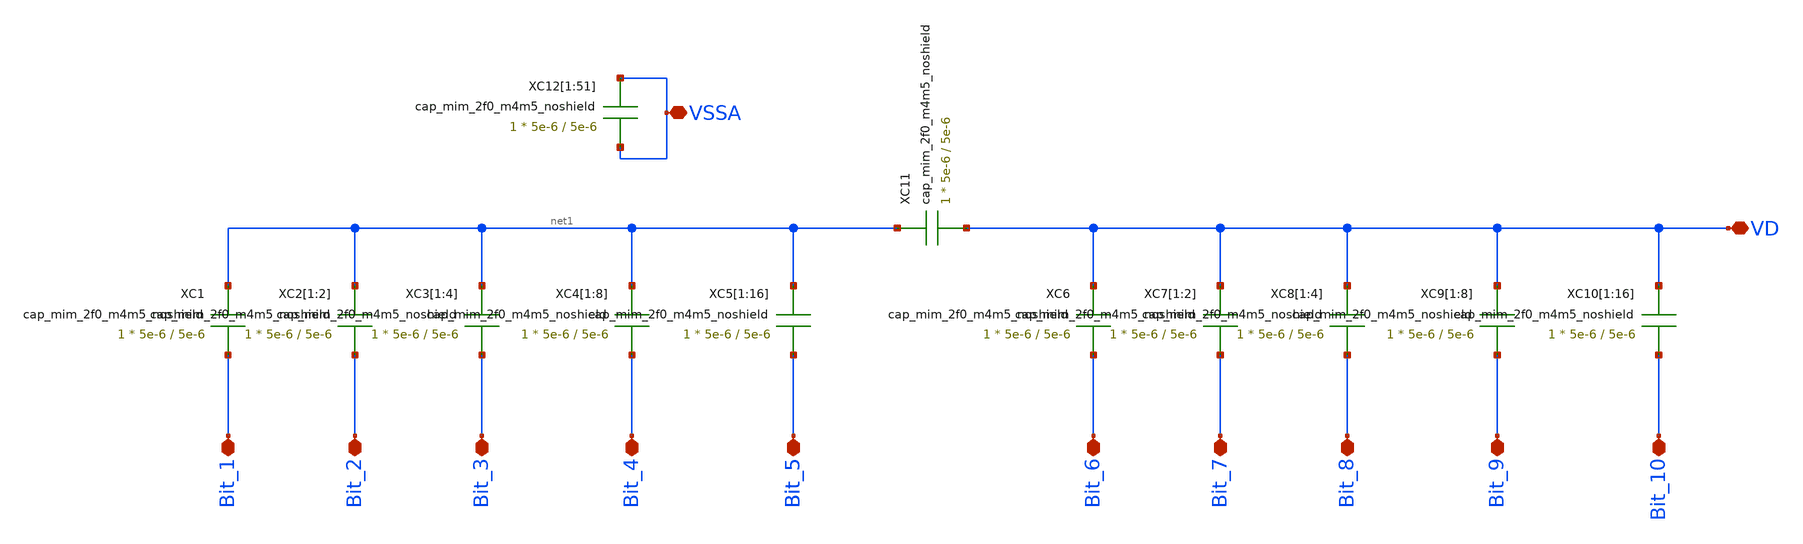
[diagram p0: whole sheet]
** sch_path: SAR_ADC/Differential_capacitive_DAC/xschem/Differential_capacitive_DAC_array.sch
**.subckt Differential_capacitive_DAC_array Bit_1 Bit_2 Bit_3 Bit_4 Bit_5 Bit_6 Bit_7 Bit_8 Bit_9
*+ Bit_10 VD Bit_5 VSSA
*.iopin Bit_1
*.iopin Bit_2
*.iopin Bit_3
*.iopin Bit_4
*.iopin Bit_5
*.iopin Bit_6
*.iopin Bit_7
*.iopin Bit_8
*.iopin Bit_9
*.iopin Bit_10
*.iopin VD
*.iopin Bit_5
*.iopin VSSA
XC1 net1 Bit_1 cap_mim_2f0_m4m5_noshield c_width=5e-6 c_length=5e-6 m=1
XC2[1] net1 Bit_2 cap_mim_2f0_m4m5_noshield c_width=5e-6 c_length=5e-6 m=1
XC2[2] net1 Bit_2 cap_mim_2f0_m4m5_noshield c_width=5e-6 c_length=5e-6 m=1
XC3[1] net1 Bit_3 cap_mim_2f0_m4m5_noshield c_width=5e-6 c_length=5e-6 m=1
XC3[2] net1 Bit_3 cap_mim_2f0_m4m5_noshield c_width=5e-6 c_length=5e-6 m=1
XC3[3] net1 Bit_3 cap_mim_2f0_m4m5_noshield c_width=5e-6 c_length=5e-6 m=1
XC3[4] net1 Bit_3 cap_mim_2f0_m4m5_noshield c_width=5e-6 c_length=5e-6 m=1
XC4[1] net1 Bit_4 cap_mim_2f0_m4m5_noshield c_width=5e-6 c_length=5e-6 m=1
XC4[2] net1 Bit_4 cap_mim_2f0_m4m5_noshield c_width=5e-6 c_length=5e-6 m=1
XC4[3] net1 Bit_4 cap_mim_2f0_m4m5_noshield c_width=5e-6 c_length=5e-6 m=1
XC4[4] net1 Bit_4 cap_mim_2f0_m4m5_noshield c_width=5e-6 c_length=5e-6 m=1
XC4[5] net1 Bit_4 cap_mim_2f0_m4m5_noshield c_width=5e-6 c_length=5e-6 m=1
XC4[6] net1 Bit_4 cap_mim_2f0_m4m5_noshield c_width=5e-6 c_length=5e-6 m=1
XC4[7] net1 Bit_4 cap_mim_2f0_m4m5_noshield c_width=5e-6 c_length=5e-6 m=1
XC4[8] net1 Bit_4 cap_mim_2f0_m4m5_noshield c_width=5e-6 c_length=5e-6 m=1
XC5[1] net1 Bit_5 cap_mim_2f0_m4m5_noshield c_width=5e-6 c_length=5e-6 m=1
XC5[2] net1 Bit_5 cap_mim_2f0_m4m5_noshield c_width=5e-6 c_length=5e-6 m=1
XC5[3] net1 Bit_5 cap_mim_2f0_m4m5_noshield c_width=5e-6 c_length=5e-6 m=1
XC5[4] net1 Bit_5 cap_mim_2f0_m4m5_noshield c_width=5e-6 c_length=5e-6 m=1
XC5[5] net1 Bit_5 cap_mim_2f0_m4m5_noshield c_width=5e-6 c_length=5e-6 m=1
XC5[6] net1 Bit_5 cap_mim_2f0_m4m5_noshield c_width=5e-6 c_length=5e-6 m=1
XC5[7] net1 Bit_5 cap_mim_2f0_m4m5_noshield c_width=5e-6 c_length=5e-6 m=1
XC5[8] net1 Bit_5 cap_mim_2f0_m4m5_noshield c_width=5e-6 c_length=5e-6 m=1
XC5[9] net1 Bit_5 cap_mim_2f0_m4m5_noshield c_width=5e-6 c_length=5e-6 m=1
XC5[10] net1 Bit_5 cap_mim_2f0_m4m5_noshield c_width=5e-6 c_length=5e-6 m=1
XC5[11] net1 Bit_5 cap_mim_2f0_m4m5_noshield c_width=5e-6 c_length=5e-6 m=1
XC5[12] net1 Bit_5 cap_mim_2f0_m4m5_noshield c_width=5e-6 c_length=5e-6 m=1
XC5[13] net1 Bit_5 cap_mim_2f0_m4m5_noshield c_width=5e-6 c_length=5e-6 m=1
XC5[14] net1 Bit_5 cap_mim_2f0_m4m5_noshield c_width=5e-6 c_length=5e-6 m=1
XC5[15] net1 Bit_5 cap_mim_2f0_m4m5_noshield c_width=5e-6 c_length=5e-6 m=1
XC5[16] net1 Bit_5 cap_mim_2f0_m4m5_noshield c_width=5e-6 c_length=5e-6 m=1
XC6 VD Bit_6 cap_mim_2f0_m4m5_noshield c_width=5e-6 c_length=5e-6 m=1
XC7[1] VD Bit_7 cap_mim_2f0_m4m5_noshield c_width=5e-6 c_length=5e-6 m=1
XC7[2] VD Bit_7 cap_mim_2f0_m4m5_noshield c_width=5e-6 c_length=5e-6 m=1
XC8[1] VD Bit_8 cap_mim_2f0_m4m5_noshield c_width=5e-6 c_length=5e-6 m=1
XC8[2] VD Bit_8 cap_mim_2f0_m4m5_noshield c_width=5e-6 c_length=5e-6 m=1
XC8[3] VD Bit_8 cap_mim_2f0_m4m5_noshield c_width=5e-6 c_length=5e-6 m=1
XC8[4] VD Bit_8 cap_mim_2f0_m4m5_noshield c_width=5e-6 c_length=5e-6 m=1
XC9[1] VD Bit_9 cap_mim_2f0_m4m5_noshield c_width=5e-6 c_length=5e-6 m=1
XC9[2] VD Bit_9 cap_mim_2f0_m4m5_noshield c_width=5e-6 c_length=5e-6 m=1
XC9[3] VD Bit_9 cap_mim_2f0_m4m5_noshield c_width=5e-6 c_length=5e-6 m=1
XC9[4] VD Bit_9 cap_mim_2f0_m4m5_noshield c_width=5e-6 c_length=5e-6 m=1
XC9[5] VD Bit_9 cap_mim_2f0_m4m5_noshield c_width=5e-6 c_length=5e-6 m=1
XC9[6] VD Bit_9 cap_mim_2f0_m4m5_noshield c_width=5e-6 c_length=5e-6 m=1
XC9[7] VD Bit_9 cap_mim_2f0_m4m5_noshield c_width=5e-6 c_length=5e-6 m=1
XC9[8] VD Bit_9 cap_mim_2f0_m4m5_noshield c_width=5e-6 c_length=5e-6 m=1
XC10[1] VD Bit_10 cap_mim_2f0_m4m5_noshield c_width=5e-6 c_length=5e-6 m=1
XC10[2] VD Bit_10 cap_mim_2f0_m4m5_noshield c_width=5e-6 c_length=5e-6 m=1
XC10[3] VD Bit_10 cap_mim_2f0_m4m5_noshield c_width=5e-6 c_length=5e-6 m=1
XC10[4] VD Bit_10 cap_mim_2f0_m4m5_noshield c_width=5e-6 c_length=5e-6 m=1
XC10[5] VD Bit_10 cap_mim_2f0_m4m5_noshield c_width=5e-6 c_length=5e-6 m=1
XC10[6] VD Bit_10 cap_mim_2f0_m4m5_noshield c_width=5e-6 c_length=5e-6 m=1
XC10[7] VD Bit_10 cap_mim_2f0_m4m5_noshield c_width=5e-6 c_length=5e-6 m=1
XC10[8] VD Bit_10 cap_mim_2f0_m4m5_noshield c_width=5e-6 c_length=5e-6 m=1
XC10[9] VD Bit_10 cap_mim_2f0_m4m5_noshield c_width=5e-6 c_length=5e-6 m=1
XC10[10] VD Bit_10 cap_mim_2f0_m4m5_noshield c_width=5e-6 c_length=5e-6 m=1
XC10[11] VD Bit_10 cap_mim_2f0_m4m5_noshield c_width=5e-6 c_length=5e-6 m=1
XC10[12] VD Bit_10 cap_mim_2f0_m4m5_noshield c_width=5e-6 c_length=5e-6 m=1
XC10[13] VD Bit_10 cap_mim_2f0_m4m5_noshield c_width=5e-6 c_length=5e-6 m=1
XC10[14] VD Bit_10 cap_mim_2f0_m4m5_noshield c_width=5e-6 c_length=5e-6 m=1
XC10[15] VD Bit_10 cap_mim_2f0_m4m5_noshield c_width=5e-6 c_length=5e-6 m=1
XC10[16] VD Bit_10 cap_mim_2f0_m4m5_noshield c_width=5e-6 c_length=5e-6 m=1
XC11 net1 VD cap_mim_2f0_m4m5_noshield c_width=5e-6 c_length=5e-6 m=1
XC12[1] VSSA VSSA cap_mim_2f0_m4m5_noshield c_width=5e-6 c_length=5e-6 m=1
XC12[2] VSSA VSSA cap_mim_2f0_m4m5_noshield c_width=5e-6 c_length=5e-6 m=1
XC12[3] VSSA VSSA cap_mim_2f0_m4m5_noshield c_width=5e-6 c_length=5e-6 m=1
XC12[4] VSSA VSSA cap_mim_2f0_m4m5_noshield c_width=5e-6 c_length=5e-6 m=1
XC12[5] VSSA VSSA cap_mim_2f0_m4m5_noshield c_width=5e-6 c_length=5e-6 m=1
XC12[6] VSSA VSSA cap_mim_2f0_m4m5_noshield c_width=5e-6 c_length=5e-6 m=1
XC12[7] VSSA VSSA cap_mim_2f0_m4m5_noshield c_width=5e-6 c_length=5e-6 m=1
XC12[8] VSSA VSSA cap_mim_2f0_m4m5_noshield c_width=5e-6 c_length=5e-6 m=1
XC12[9] VSSA VSSA cap_mim_2f0_m4m5_noshield c_width=5e-6 c_length=5e-6 m=1
XC12[10] VSSA VSSA cap_mim_2f0_m4m5_noshield c_width=5e-6 c_length=5e-6 m=1
XC12[11] VSSA VSSA cap_mim_2f0_m4m5_noshield c_width=5e-6 c_length=5e-6 m=1
XC12[12] VSSA VSSA cap_mim_2f0_m4m5_noshield c_width=5e-6 c_length=5e-6 m=1
XC12[13] VSSA VSSA cap_mim_2f0_m4m5_noshield c_width=5e-6 c_length=5e-6 m=1
XC12[14] VSSA VSSA cap_mim_2f0_m4m5_noshield c_width=5e-6 c_length=5e-6 m=1
XC12[15] VSSA VSSA cap_mim_2f0_m4m5_noshield c_width=5e-6 c_length=5e-6 m=1
XC12[16] VSSA VSSA cap_mim_2f0_m4m5_noshield c_width=5e-6 c_length=5e-6 m=1
XC12[17] VSSA VSSA cap_mim_2f0_m4m5_noshield c_width=5e-6 c_length=5e-6 m=1
XC12[18] VSSA VSSA cap_mim_2f0_m4m5_noshield c_width=5e-6 c_length=5e-6 m=1
XC12[19] VSSA VSSA cap_mim_2f0_m4m5_noshield c_width=5e-6 c_length=5e-6 m=1
XC12[20] VSSA VSSA cap_mim_2f0_m4m5_noshield c_width=5e-6 c_length=5e-6 m=1
XC12[21] VSSA VSSA cap_mim_2f0_m4m5_noshield c_width=5e-6 c_length=5e-6 m=1
XC12[22] VSSA VSSA cap_mim_2f0_m4m5_noshield c_width=5e-6 c_length=5e-6 m=1
XC12[23] VSSA VSSA cap_mim_2f0_m4m5_noshield c_width=5e-6 c_length=5e-6 m=1
XC12[24] VSSA VSSA cap_mim_2f0_m4m5_noshield c_width=5e-6 c_length=5e-6 m=1
XC12[25] VSSA VSSA cap_mim_2f0_m4m5_noshield c_width=5e-6 c_length=5e-6 m=1
XC12[26] VSSA VSSA cap_mim_2f0_m4m5_noshield c_width=5e-6 c_length=5e-6 m=1
XC12[27] VSSA VSSA cap_mim_2f0_m4m5_noshield c_width=5e-6 c_length=5e-6 m=1
XC12[28] VSSA VSSA cap_mim_2f0_m4m5_noshield c_width=5e-6 c_length=5e-6 m=1
XC12[29] VSSA VSSA cap_mim_2f0_m4m5_noshield c_width=5e-6 c_length=5e-6 m=1
XC12[30] VSSA VSSA cap_mim_2f0_m4m5_noshield c_width=5e-6 c_length=5e-6 m=1
XC12[31] VSSA VSSA cap_mim_2f0_m4m5_noshield c_width=5e-6 c_length=5e-6 m=1
XC12[32] VSSA VSSA cap_mim_2f0_m4m5_noshield c_width=5e-6 c_length=5e-6 m=1
XC12[33] VSSA VSSA cap_mim_2f0_m4m5_noshield c_width=5e-6 c_length=5e-6 m=1
XC12[34] VSSA VSSA cap_mim_2f0_m4m5_noshield c_width=5e-6 c_length=5e-6 m=1
XC12[35] VSSA VSSA cap_mim_2f0_m4m5_noshield c_width=5e-6 c_length=5e-6 m=1
XC12[36] VSSA VSSA cap_mim_2f0_m4m5_noshield c_width=5e-6 c_length=5e-6 m=1
XC12[37] VSSA VSSA cap_mim_2f0_m4m5_noshield c_width=5e-6 c_length=5e-6 m=1
XC12[38] VSSA VSSA cap_mim_2f0_m4m5_noshield c_width=5e-6 c_length=5e-6 m=1
XC12[39] VSSA VSSA cap_mim_2f0_m4m5_noshield c_width=5e-6 c_length=5e-6 m=1
XC12[40] VSSA VSSA cap_mim_2f0_m4m5_noshield c_width=5e-6 c_length=5e-6 m=1
XC12[41] VSSA VSSA cap_mim_2f0_m4m5_noshield c_width=5e-6 c_length=5e-6 m=1
XC12[42] VSSA VSSA cap_mim_2f0_m4m5_noshield c_width=5e-6 c_length=5e-6 m=1
XC12[43] VSSA VSSA cap_mim_2f0_m4m5_noshield c_width=5e-6 c_length=5e-6 m=1
XC12[44] VSSA VSSA cap_mim_2f0_m4m5_noshield c_width=5e-6 c_length=5e-6 m=1
XC12[45] VSSA VSSA cap_mim_2f0_m4m5_noshield c_width=5e-6 c_length=5e-6 m=1
XC12[46] VSSA VSSA cap_mim_2f0_m4m5_noshield c_width=5e-6 c_length=5e-6 m=1
XC12[47] VSSA VSSA cap_mim_2f0_m4m5_noshield c_width=5e-6 c_length=5e-6 m=1
XC12[48] VSSA VSSA cap_mim_2f0_m4m5_noshield c_width=5e-6 c_length=5e-6 m=1
XC12[49] VSSA VSSA cap_mim_2f0_m4m5_noshield c_width=5e-6 c_length=5e-6 m=1
XC12[50] VSSA VSSA cap_mim_2f0_m4m5_noshield c_width=5e-6 c_length=5e-6 m=1
XC12[51] VSSA VSSA cap_mim_2f0_m4m5_noshield c_width=5e-6 c_length=5e-6 m=1
**.ends
.end
